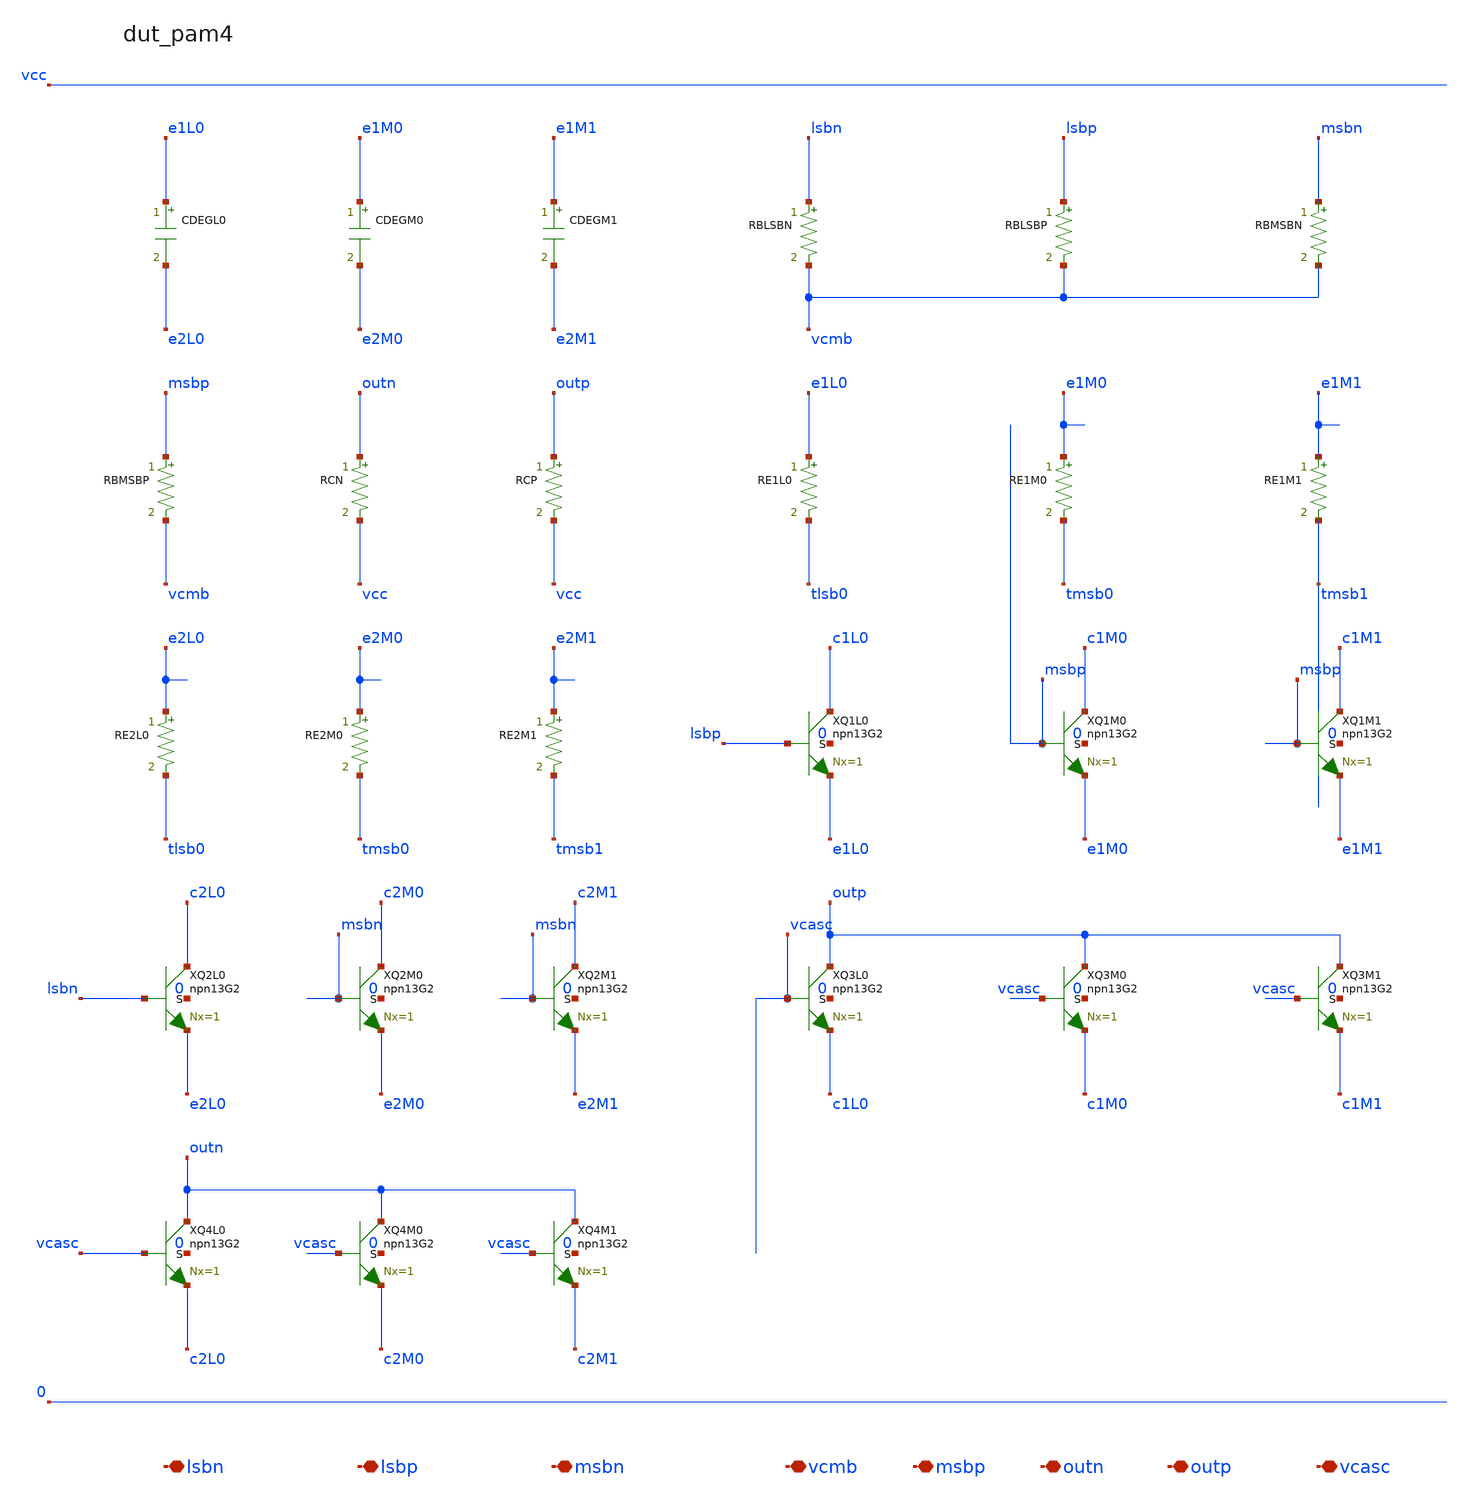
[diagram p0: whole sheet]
** sch_path: analog-db/drawings/pam4-driver-2-bit-dac-HBT/ported-netlists/schematics/dut_pam4_flat.sch
**.subckt dut_pam4_flat lsbn lsbp msbn vcmb msbp outn outp vcasc
*.iopin lsbn
*.iopin lsbp
*.iopin msbn
*.iopin vcmb
*.iopin msbp
*.iopin outn
*.iopin outp
*.iopin vcasc
XQ1L0 c1L0 lsbp e1L0 0 npn13G2 Nx=1
XQ2L0 c2L0 lsbn e2L0 0 npn13G2 Nx=1
XQ3L0 outp vcasc c1L0 0 npn13G2 Nx=1
XQ4L0 outn vcasc c2L0 0 npn13G2 Nx=1
RE1L0 e1L0 tlsb0 2.5 m=1
RE2L0 e2L0 tlsb0 2.5 m=1
CDEGL0 e1L0 e2L0 20f m=1
XQ1M0 c1M0 msbp e1M0 0 npn13G2 Nx=1
XQ2M0 c2M0 msbn e2M0 0 npn13G2 Nx=1
XQ3M0 outp vcasc c1M0 0 npn13G2 Nx=1
XQ4M0 outn vcasc c2M0 0 npn13G2 Nx=1
RE1M0 e1M0 tmsb0 2.5 m=1
RE2M0 e2M0 tmsb0 2.5 m=1
CDEGM0 e1M0 e2M0 20f m=1
XQ1M1 c1M1 msbp e1M1 0 npn13G2 Nx=1
XQ2M1 c2M1 msbn e2M1 0 npn13G2 Nx=1
XQ3M1 outp vcasc c1M1 0 npn13G2 Nx=1
XQ4M1 outn vcasc c2M1 0 npn13G2 Nx=1
RE1M1 e1M1 tmsb1 2.5 m=1
RE2M1 e2M1 tmsb1 2.5 m=1
CDEGM1 e1M1 e2M1 20f m=1
RCP outp vcc 50 m=1
RCN outn vcc 50 m=1
RBLSBP lsbp vcmb 50 m=1
RBLSBN lsbn vcmb 50 m=1
RBMSBP msbp vcmb 50 m=1
RBMSBN msbn vcmb 50 m=1
**.ends
.end
